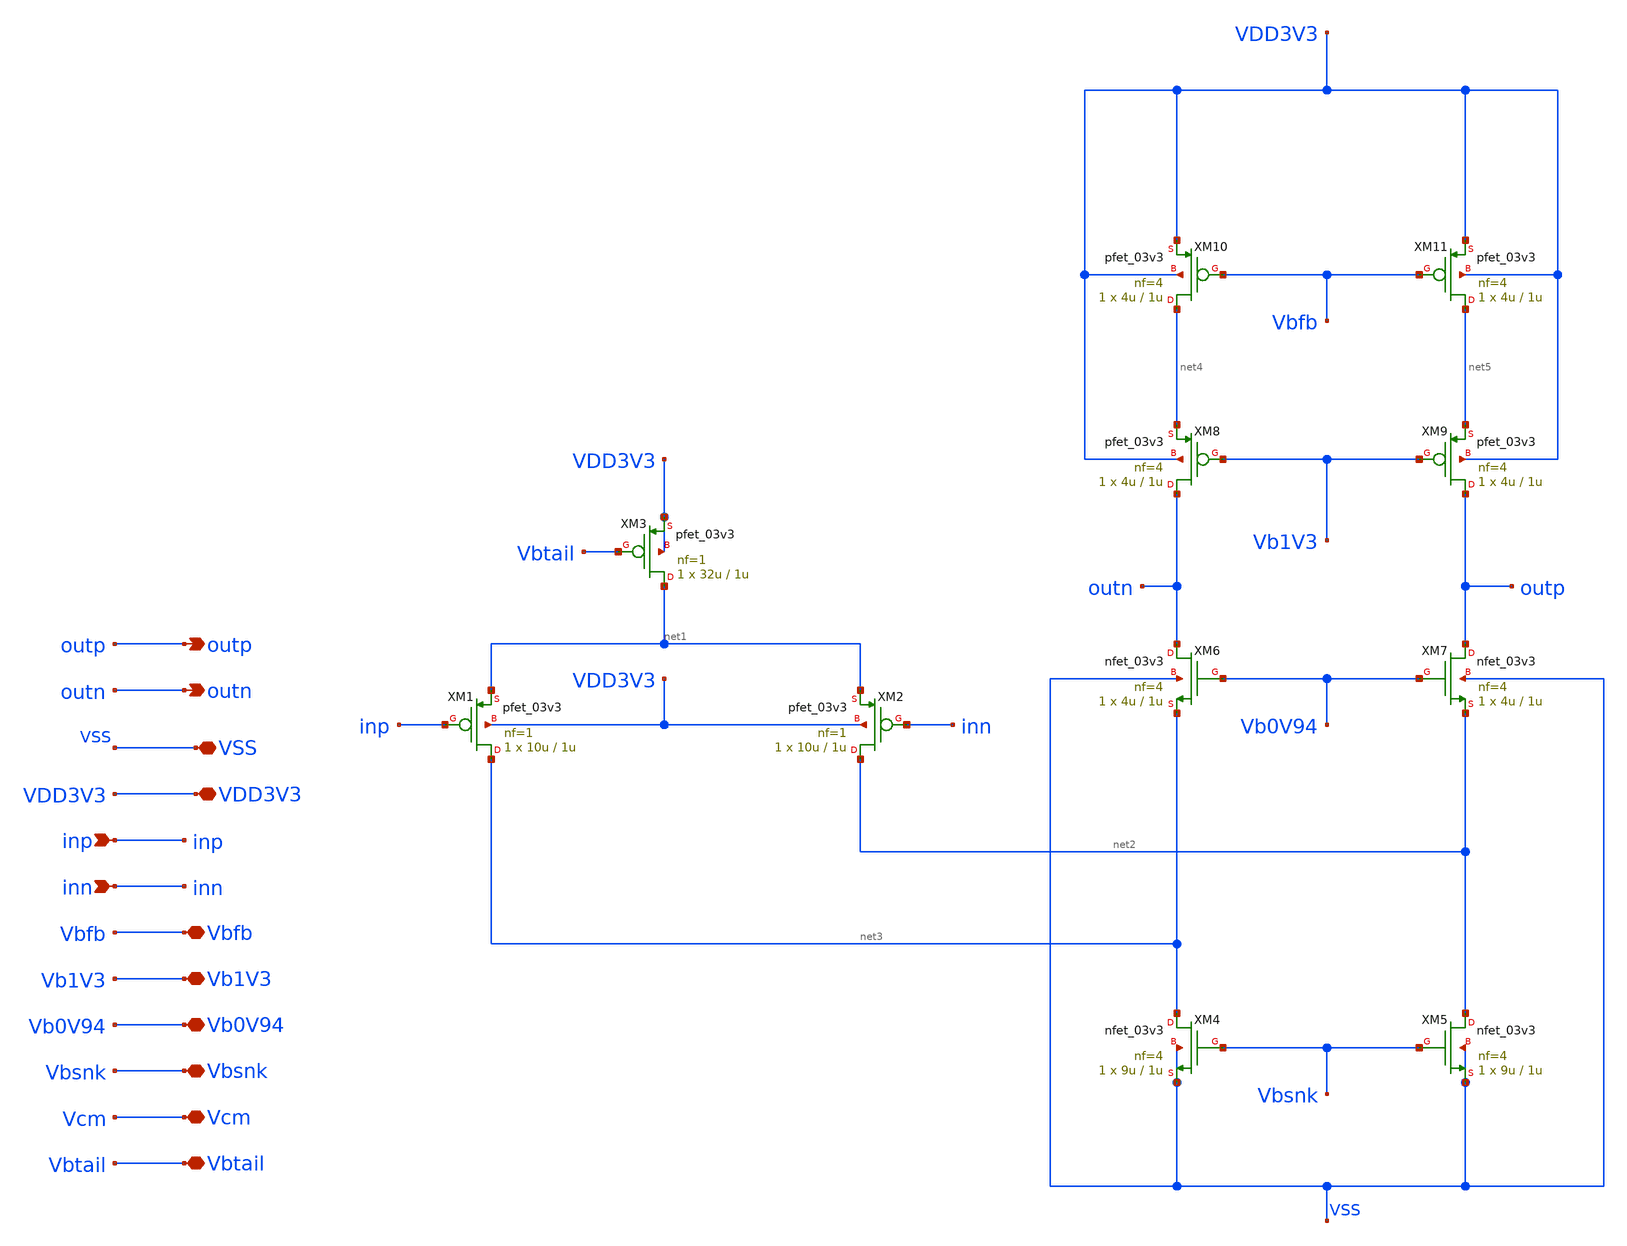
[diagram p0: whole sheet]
** sch_path: designs/libs/core_pga/folded_cascode/folded.sch
**.subckt folded outp outn VSS VDD3V3 inp inn Vb1V3 Vb0V94 Vcm Vbfb Vbsnk Vbtail
*.opin outp
*.opin outn
*.iopin VSS
*.iopin VDD3V3
*.ipin inp
*.ipin inn
*.iopin Vb1V3
*.iopin Vb0V94
*.iopin Vcm
*.iopin Vbfb
*.iopin Vbsnk
*.iopin Vbtail
XM1 net3 inp net1 VDD3V3 pfet_03v3 L=1u W=10u nf=1 ad='int((nf+1)/2) * W/nf * 0.18u' as='int((nf+2)/2) * W/nf * 0.18u'
+ pd='2*int((nf+1)/2) * (W/nf + 0.18u)' ps='2*int((nf+2)/2) * (W/nf + 0.18u)' nrd='0.18u / W' nrs='0.18u / W'
+ sa=0 sb=0 sd=0 m=1
XM2 net2 inn net1 VDD3V3 pfet_03v3 L=1u W=10u nf=1 ad='int((nf+1)/2) * W/nf * 0.18u' as='int((nf+2)/2) * W/nf * 0.18u'
+ pd='2*int((nf+1)/2) * (W/nf + 0.18u)' ps='2*int((nf+2)/2) * (W/nf + 0.18u)' nrd='0.18u / W' nrs='0.18u / W'
+ sa=0 sb=0 sd=0 m=1
XM6 outn Vb0V94 net3 VSS nfet_03v3 L=1u W=4u nf=4 ad='int((nf+1)/2) * W/nf * 0.18u' as='int((nf+2)/2) * W/nf * 0.18u'
+ pd='2*int((nf+1)/2) * (W/nf + 0.18u)' ps='2*int((nf+2)/2) * (W/nf + 0.18u)' nrd='0.18u / W' nrs='0.18u / W'
+ sa=0 sb=0 sd=0 m=1
XM7 outp Vb0V94 net2 VSS nfet_03v3 L=1u W=4u nf=4 ad='int((nf+1)/2) * W/nf * 0.18u' as='int((nf+2)/2) * W/nf * 0.18u'
+ pd='2*int((nf+1)/2) * (W/nf + 0.18u)' ps='2*int((nf+2)/2) * (W/nf + 0.18u)' nrd='0.18u / W' nrs='0.18u / W'
+ sa=0 sb=0 sd=0 m=1
XM8 outn Vb1V3 net4 VDD3V3 pfet_03v3 L=1u W=4u nf=4 ad='int((nf+1)/2) * W/nf * 0.18u' as='int((nf+2)/2) * W/nf * 0.18u'
+ pd='2*int((nf+1)/2) * (W/nf + 0.18u)' ps='2*int((nf+2)/2) * (W/nf + 0.18u)' nrd='0.18u / W' nrs='0.18u / W'
+ sa=0 sb=0 sd=0 m=1
XM9 outp Vb1V3 net5 VDD3V3 pfet_03v3 L=1u W=4u nf=4 ad='int((nf+1)/2) * W/nf * 0.18u' as='int((nf+2)/2) * W/nf * 0.18u'
+ pd='2*int((nf+1)/2) * (W/nf + 0.18u)' ps='2*int((nf+2)/2) * (W/nf + 0.18u)' nrd='0.18u / W' nrs='0.18u / W'
+ sa=0 sb=0 sd=0 m=1
XM3 net1 Vbtail VDD3V3 VDD3V3 pfet_03v3 L=1u W=32u nf=1 ad='int((nf+1)/2) * W/nf * 0.18u' as='int((nf+2)/2) * W/nf * 0.18u'
+ pd='2*int((nf+1)/2) * (W/nf + 0.18u)' ps='2*int((nf+2)/2) * (W/nf + 0.18u)' nrd='0.18u / W' nrs='0.18u / W'
+ sa=0 sb=0 sd=0 m=1
XM4 net3 Vbsnk VSS VSS nfet_03v3 L=1u W=9u nf=4 ad='int((nf+1)/2) * W/nf * 0.18u' as='int((nf+2)/2) * W/nf * 0.18u'
+ pd='2*int((nf+1)/2) * (W/nf + 0.18u)' ps='2*int((nf+2)/2) * (W/nf + 0.18u)' nrd='0.18u / W' nrs='0.18u / W'
+ sa=0 sb=0 sd=0 m=1
XM5 net2 Vbsnk VSS VSS nfet_03v3 L=1u W=9u nf=4 ad='int((nf+1)/2) * W/nf * 0.18u' as='int((nf+2)/2) * W/nf * 0.18u'
+ pd='2*int((nf+1)/2) * (W/nf + 0.18u)' ps='2*int((nf+2)/2) * (W/nf + 0.18u)' nrd='0.18u / W' nrs='0.18u / W'
+ sa=0 sb=0 sd=0 m=1
XM10 net4 Vbfb VDD3V3 VDD3V3 pfet_03v3 L=1u W=4u nf=4 ad='int((nf+1)/2) * W/nf * 0.18u' as='int((nf+2)/2) * W/nf * 0.18u'
+ pd='2*int((nf+1)/2) * (W/nf + 0.18u)' ps='2*int((nf+2)/2) * (W/nf + 0.18u)' nrd='0.18u / W' nrs='0.18u / W'
+ sa=0 sb=0 sd=0 m=1
XM11 net5 Vbfb VDD3V3 VDD3V3 pfet_03v3 L=1u W=4u nf=4 ad='int((nf+1)/2) * W/nf * 0.18u' as='int((nf+2)/2) * W/nf * 0.18u'
+ pd='2*int((nf+1)/2) * (W/nf + 0.18u)' ps='2*int((nf+2)/2) * (W/nf + 0.18u)' nrd='0.18u / W' nrs='0.18u / W'
+ sa=0 sb=0 sd=0 m=1
**.ends
.end
